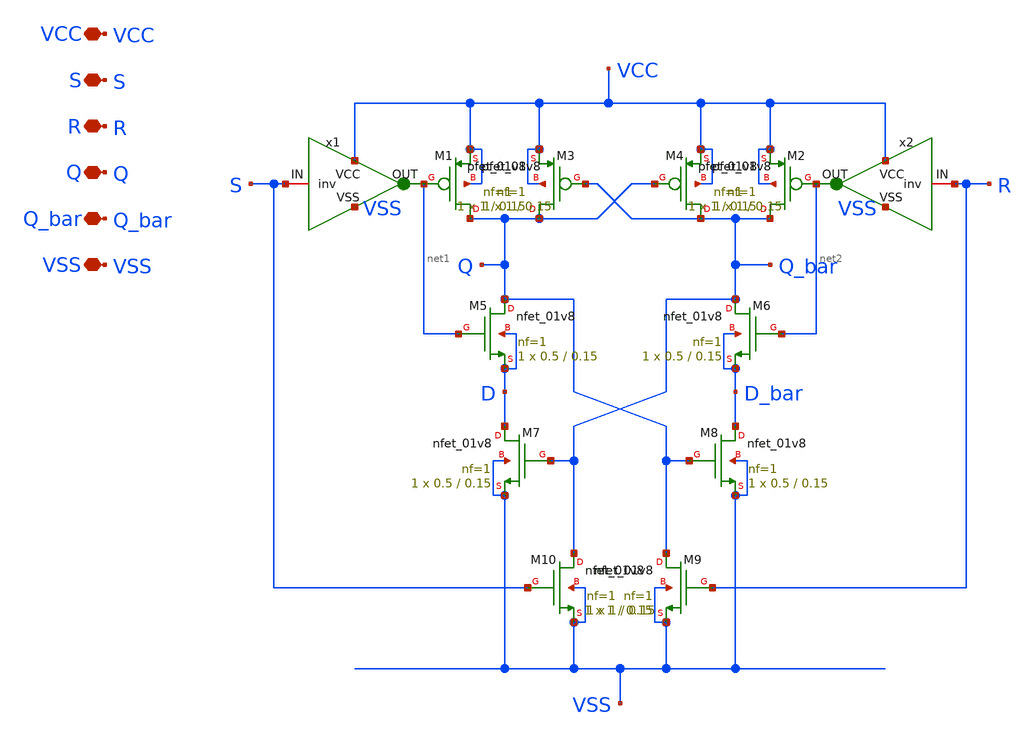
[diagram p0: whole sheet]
** sch_path: RS_latch/RS_latch.sch
**.subckt RS_latch VCC VSS S R Q Q_bar
*.iopin VCC
*.iopin VSS
*.iopin S
*.iopin R
*.iopin Q
*.iopin Q_bar
XM3 Q Q_bar VCC VCC sky130_fd_pr__pfet_01v8 L=0.15 W=1 nf=1 ad='int((nf+1)/2) * W/nf * 0.29' as='int((nf+2)/2) * W/nf * 0.29'
+ pd='2*int((nf+1)/2) * (W/nf + 0.29)' ps='2*int((nf+2)/2) * (W/nf + 0.29)' nrd='0.29 / W' nrs='0.29 / W'
+ sa=0 sb=0 sd=0 mult=1 m=1
XM1 Q net1 VCC VCC sky130_fd_pr__pfet_01v8 L=0.15 W=1 nf=1 ad='int((nf+1)/2) * W/nf * 0.29' as='int((nf+2)/2) * W/nf * 0.29'
+ pd='2*int((nf+1)/2) * (W/nf + 0.29)' ps='2*int((nf+2)/2) * (W/nf + 0.29)' nrd='0.29 / W' nrs='0.29 / W'
+ sa=0 sb=0 sd=0 mult=1 m=1
XM2 Q_bar net2 VCC VCC sky130_fd_pr__pfet_01v8 L=0.15 W=1 nf=1 ad='int((nf+1)/2) * W/nf * 0.29' as='int((nf+2)/2) * W/nf * 0.29'
+ pd='2*int((nf+1)/2) * (W/nf + 0.29)' ps='2*int((nf+2)/2) * (W/nf + 0.29)' nrd='0.29 / W' nrs='0.29 / W'
+ sa=0 sb=0 sd=0 mult=1 m=1
XM4 Q_bar Q VCC VCC sky130_fd_pr__pfet_01v8 L=0.15 W=1 nf=1 ad='int((nf+1)/2) * W/nf * 0.29' as='int((nf+2)/2) * W/nf * 0.29'
+ pd='2*int((nf+1)/2) * (W/nf + 0.29)' ps='2*int((nf+2)/2) * (W/nf + 0.29)' nrd='0.29 / W' nrs='0.29 / W'
+ sa=0 sb=0 sd=0 mult=1 m=1
XM5 Q net1 D D sky130_fd_pr__nfet_01v8 L=0.15 W=0.5 nf=1 ad='int((1 + 1)/2) * 0.5 / 1 * 0.29' as='int((1 + 2)/2) * 0.5 / 1 * 0.29'
+ pd='2*int((1 + 1)/2) * (0.5 / 1 + 0.29)' ps='2*int((1 + 2)/2) * (0.5 / 1 + 0.29)' nrd='0.29 / 0.5 ' nrs='0.29 / 0.5 '
+ sa=0 sb=0 sd=0 mult=1 m=1
XM6 Q_bar net2 D_bar D_bar sky130_fd_pr__nfet_01v8 L=0.15 W=0.5 nf=1 ad='int((1 + 1)/2) * 0.5 / 1 * 0.29'
+ as='int((1 + 2)/2) * 0.5 / 1 * 0.29' pd='2*int((1 + 1)/2) * (0.5 / 1 + 0.29)' ps='2*int((1 + 2)/2) * (0.5 / 1 + 0.29)'
+ nrd='0.29 / 0.5 ' nrs='0.29 / 0.5 ' sa=0 sb=0 sd=0 mult=1 m=1
XM7 D Q_bar VSS VSS sky130_fd_pr__nfet_01v8 L=0.15 W=0.5 nf=1 ad='int((1 + 1)/2) * 0.5 / 1 * 0.29' as='int((1 + 2)/2) * 0.5 / 1 * 0.29'
+ pd='2*int((1 + 1)/2) * (0.5 / 1 + 0.29)' ps='2*int((1 + 2)/2) * (0.5 / 1 + 0.29)' nrd='0.29 / 0.5 ' nrs='0.29 / 0.5 '
+ sa=0 sb=0 sd=0 mult=1 m=1
XM8 D_bar Q VSS VSS sky130_fd_pr__nfet_01v8 L=0.15 W=0.5 nf=1 ad='int((1 + 1)/2) * 0.5 / 1 * 0.29' as='int((1 + 2)/2) * 0.5 / 1 * 0.29'
+ pd='2*int((1 + 1)/2) * (0.5 / 1 + 0.29)' ps='2*int((1 + 2)/2) * (0.5 / 1 + 0.29)' nrd='0.29 / 0.5 ' nrs='0.29 / 0.5 '
+ sa=0 sb=0 sd=0 mult=1 m=1
XM10 Q_bar S VSS VSS sky130_fd_pr__nfet_01v8 L=0.15 W=1 nf=1 ad='int((1 + 1)/2) * 1 / 1 * 0.29' as='int((1 + 2)/2) * 1 / 1 * 0.29'
+ pd='2*int((1 + 1)/2) * (1 / 1 + 0.29)' ps='2*int((1 + 2)/2) * (1 / 1 + 0.29)' nrd='0.29 / 1 ' nrs='0.29 / 1 '
+ sa=0 sb=0 sd=0 mult=1 m=1
XM9 Q R VSS VSS sky130_fd_pr__nfet_01v8 L=0.15 W=1 nf=1 ad='int((1 + 1)/2) * 1 / 1 * 0.29' as='int((1 + 2)/2) * 1 / 1 * 0.29'
+ pd='2*int((1 + 1)/2) * (1 / 1 + 0.29)' ps='2*int((1 + 2)/2) * (1 / 1 + 0.29)' nrd='0.29 / 1 ' nrs='0.29 / 1 '
+ sa=0 sb=0 sd=0 mult=1 m=1
x1 VCC S net1 VSS inv
x2 VCC R net2 VSS inv
**.ends

* expanding   symbol:  inv.sym # of pins=4
** sym_path: RS_latch/inv.sym
** sch_path: RS_latch/inv.sch
.subckt inv VCC IN OUT VSS
*.iopin VCC
*.iopin IN
*.iopin OUT
*.iopin VSS
XM1 OUT IN VSS VSS sky130_fd_pr__nfet_01v8 L=0.15 W=0.5 nf=1 ad='int((nf+1)/2) * W/nf * 0.29' as='int((nf+2)/2) * W/nf * 0.29'
+ pd='2*int((nf+1)/2) * (W/nf + 0.29)' ps='2*int((nf+2)/2) * (W/nf + 0.29)' nrd='0.29 / W' nrs='0.29 / W'
+ sa=0 sb=0 sd=0 mult=1 m=1
XM2 OUT IN VCC VCC sky130_fd_pr__pfet_01v8 L=0.15 W=1.05 nf=1 ad='int((nf+1)/2) * W/nf * 0.29' as='int((nf+2)/2) * W/nf * 0.29'
+ pd='2*int((nf+1)/2) * (W/nf + 0.29)' ps='2*int((nf+2)/2) * (W/nf + 0.29)' nrd='0.29 / W' nrs='0.29 / W'
+ sa=0 sb=0 sd=0 mult=1 m=1
.ends

.end
